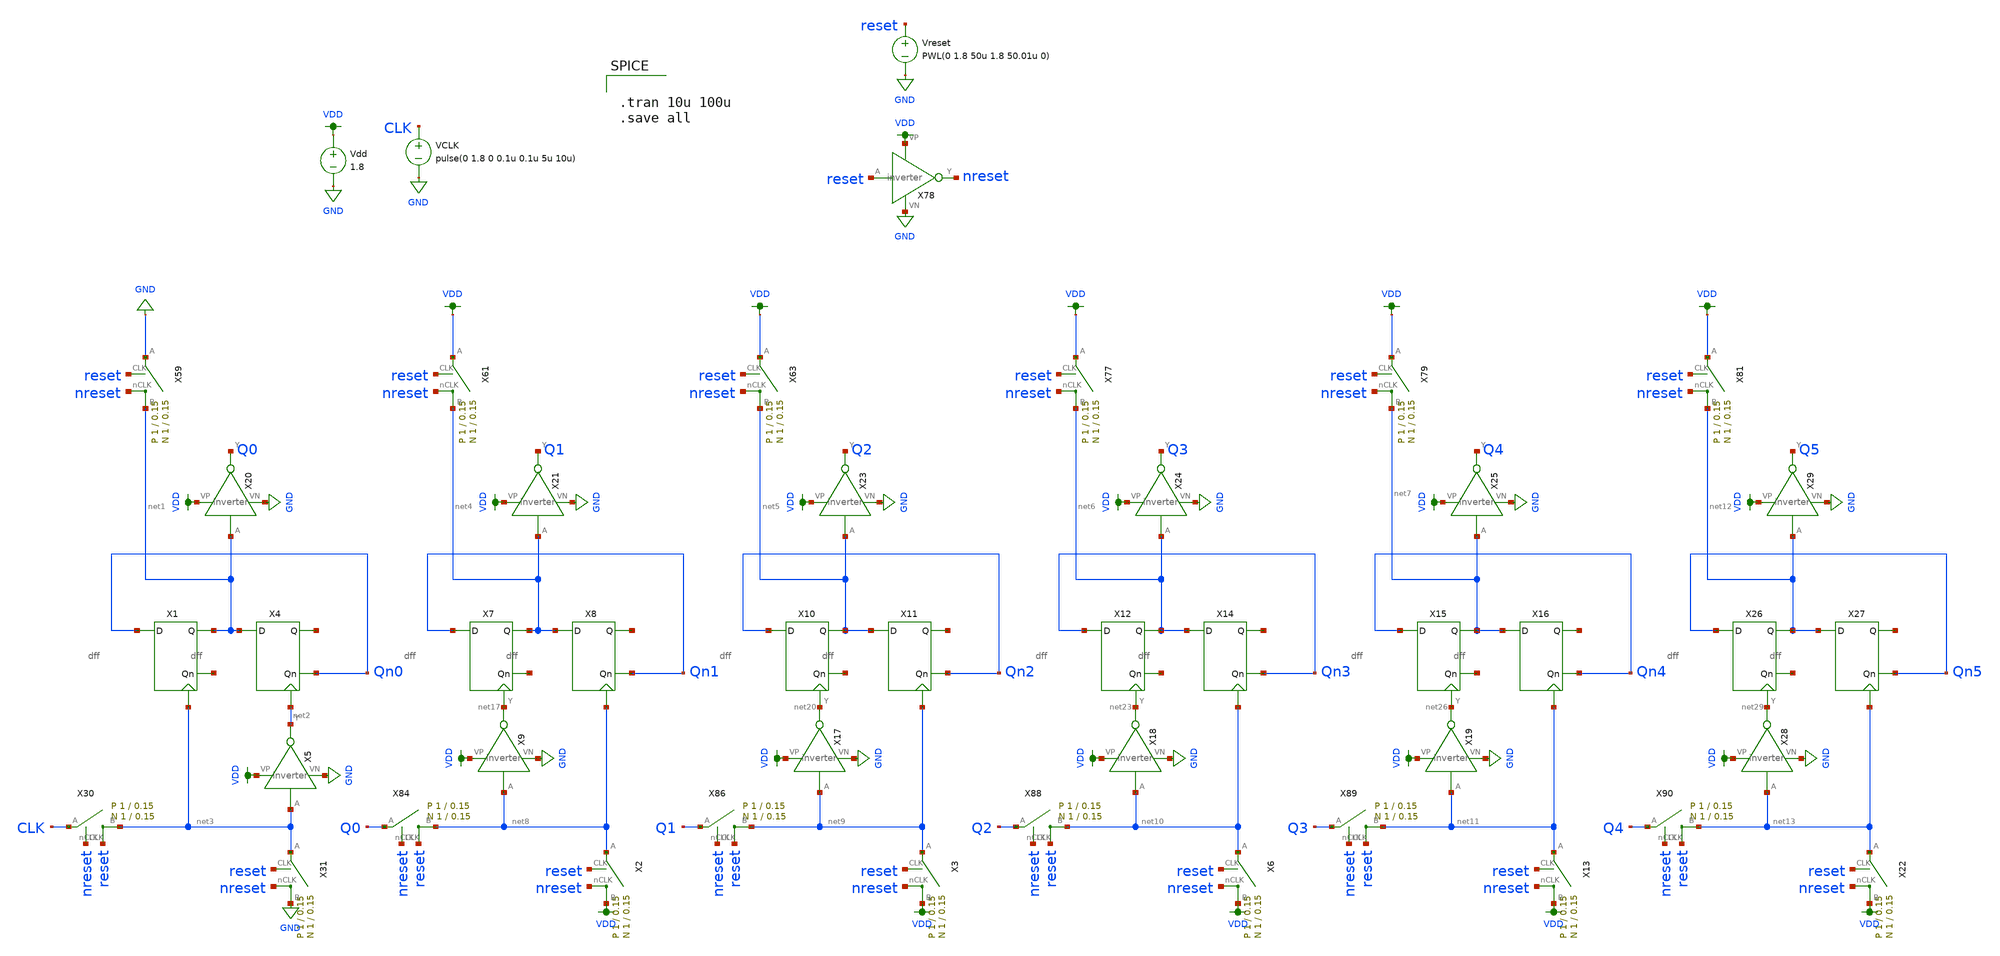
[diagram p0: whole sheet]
** sch_path: schematic/archive/counter_reset.sch
**.subckt counter_reset
Vdd VDD GND 1.8
VCLK CLK GND pulse(0 1.8 0 0.1u 0.1u 5u 10u)
X1 Qn0 net14 net1 net3 dff
X4 net1 Qn0 net15 net2 dff
X5 net3 net2 VDD GND inverter
X7 Qn1 net16 net4 net17 dff
X8 net4 Qn1 net18 net8 dff
X9 net8 net17 VDD GND inverter
X10 Qn2 net19 net5 net20 dff
X11 net5 Qn2 net21 net9 dff
X12 Qn3 net22 net6 net23 dff
X14 net6 Qn3 net24 net10 dff
X15 Qn4 net25 net7 net26 dff
X16 net7 Qn4 net27 net11 dff
X17 net9 net20 VDD GND inverter
X18 net10 net23 VDD GND inverter
X19 net11 net26 VDD GND inverter
X20 net1 Q0 VDD GND inverter
X21 net4 Q1 VDD GND inverter
X23 net5 Q2 VDD GND inverter
X24 net6 Q3 VDD GND inverter
X25 net7 Q4 VDD GND inverter
X26 Qn5 net28 net12 net29 dff
X27 net12 Qn5 net30 net13 dff
X28 net13 net29 VDD GND inverter
X29 net12 Q5 VDD GND inverter
X59 net1 GND reset nreset switch Wp=1 Lp=0.15 WW=1 LL=0.15
X61 net4 VDD reset nreset switch Wp=1 Lp=0.15 WW=1 LL=0.15
X63 net5 VDD reset nreset switch Wp=1 Lp=0.15 WW=1 LL=0.15
X77 net6 VDD reset nreset switch Wp=1 Lp=0.15 WW=1 LL=0.15
X79 net7 VDD reset nreset switch Wp=1 Lp=0.15 WW=1 LL=0.15
X81 net12 VDD reset nreset switch Wp=1 Lp=0.15 WW=1 LL=0.15
X84 net8 Q0 nreset reset switch Wp=1 Lp=0.15 WW=1 LL=0.15
X86 net9 Q1 nreset reset switch Wp=1 Lp=0.15 WW=1 LL=0.15
X88 net10 Q2 nreset reset switch Wp=1 Lp=0.15 WW=1 LL=0.15
X89 net11 Q3 nreset reset switch Wp=1 Lp=0.15 WW=1 LL=0.15
X90 net13 Q4 nreset reset switch Wp=1 Lp=0.15 WW=1 LL=0.15
Vreset reset GND PWL(0 1.8 50u 1.8 50.01u 0)
X78 reset nreset VDD GND inverter
X2 VDD net8 reset nreset switch Wp=1 Lp=0.15 WW=1 LL=0.15
X3 VDD net9 reset nreset switch Wp=1 Lp=0.15 WW=1 LL=0.15
X6 VDD net10 reset nreset switch Wp=1 Lp=0.15 WW=1 LL=0.15
X13 VDD net11 reset nreset switch Wp=1 Lp=0.15 WW=1 LL=0.15
X22 VDD net13 reset nreset switch Wp=1 Lp=0.15 WW=1 LL=0.15
X30 net3 CLK nreset reset switch Wp=1 Lp=0.15 WW=1 LL=0.15
X31 GND net3 reset nreset switch Wp=1 Lp=0.15 WW=1 LL=0.15
**** begin user architecture code


.tran 10u 100u
.save all


.option wnflag=1
.param MC_SWITCH=0.0
.lib ~/skywater/skywater-pdk/libraries/sky130_fd_pr_ngspice/latest/models/sky130.lib.spice tt

**** end user architecture code
**.ends

* expanding   symbol:  /home/madvlsi/Documents/MADVLSI-Final_Project/schematic/dff.sym # of pins=4
** sym_path: schematic/dff.sym
** sch_path: schematic/dff.sch
.subckt dff D Qn Q CLK
*.ipin D
*.iopin CLK
*.opin Qn
*.opin Q
X2 D CLK net1 VDD GND nand2
X3 net3 CLK net2 VDD GND nand2
X4 Q net2 Qn VDD GND nand2
X5 net1 Qn Q VDD GND nand2
X1 D net3 VDD GND inverter
.ends


* expanding   symbol:  /home/madvlsi/Documents/MADVLSI-Final_Project/schematic/inverter.sym # of
*+ pins=4
** sym_path: schematic/inverter.sym
** sch_path: schematic/inverter.sch
.subckt inverter A Y VP VN
*.opin Y
*.ipin A
*.iopin VP
*.iopin VN
XM3 Y A VP VDD sky130_fd_pr__pfet_01v8 L={Lp} W={Wp} nf=1 ad='int((nf+1)/2) * W/nf * 0.29' as='int((nf+2)/2) * W/nf * 0.29'
+ pd='2*int((nf+1)/2) * (W/nf + 0.29)' ps='2*int((nf+2)/2) * (W/nf + 0.29)' nrd='0.29 / W' nrs='0.29 / W'
+ sa=0 sb=0 sd=0 mult=1 m=1
XM4 Y A VP VDD sky130_fd_pr__pfet_01v8 L={Lp} W={Wp} nf=1 ad='int((nf+1)/2) * W/nf * 0.29' as='int((nf+2)/2) * W/nf * 0.29'
+ pd='2*int((nf+1)/2) * (W/nf + 0.29)' ps='2*int((nf+2)/2) * (W/nf + 0.29)' nrd='0.29 / W' nrs='0.29 / W'
+ sa=0 sb=0 sd=0 mult=1 m=1
XM5 Y A VN GND sky130_fd_pr__nfet_01v8 L={Lp} W={Wp} nf=1 ad='int((nf+1)/2) * W/nf * 0.29' as='int((nf+2)/2) * W/nf * 0.29'
+ pd='2*int((nf+1)/2) * (W/nf + 0.29)' ps='2*int((nf+2)/2) * (W/nf + 0.29)' nrd='0.29 / W' nrs='0.29 / W'
+ sa=0 sb=0 sd=0 mult=1 m=1
.ends


* expanding   symbol:  /home/madvlsi/Documents/MADVLSI-Final_Project/schematic/switch.sym # of
*+ pins=4
** sym_path: schematic/switch.sym
** sch_path: schematic/switch.sch
.subckt switch B A CLK nCLK  Wp=1 Lp=0.15 WW=1 LL=0.15
*.iopin B
*.iopin A
*.ipin CLK
*.ipin nCLK
*.ipin CLK
*.ipin CLK
*.ipin nCLK
*.ipin nCLK
XM1 A CLK B GND sky130_fd_pr__nfet_01v8 L={LL} W={WW} nf=1 ad='int((nf+1)/2) * W/nf * 0.29' as='int((nf+2)/2) * W/nf * 0.29'
+ pd='2*int((nf+1)/2) * (W/nf + 0.29)' ps='2*int((nf+2)/2) * (W/nf + 0.29)' nrd='0.29 / W' nrs='0.29 / W'
+ sa=0 sb=0 sd=0 mult=1 m=1
XM2 A nCLK B VDD sky130_fd_pr__pfet_01v8 L={Lp} W={Wp} nf=1 ad='int((nf+1)/2) * W/nf * 0.29' as='int((nf+2)/2) * W/nf * 0.29'
+ pd='2*int((nf+1)/2) * (W/nf + 0.29)' ps='2*int((nf+2)/2) * (W/nf + 0.29)' nrd='0.29 / W' nrs='0.29 / W'
+ sa=0 sb=0 sd=0 mult=1 m=1
XM3 B CLK B VDD sky130_fd_pr__pfet_01v8 L={Lp} W={Wp/2} nf=1 ad='int((nf+1)/2) * W/nf * 0.29' as='int((nf+2)/2) * W/nf * 0.29'
+ pd='2*int((nf+1)/2) * (W/nf + 0.29)' ps='2*int((nf+2)/2) * (W/nf + 0.29)' nrd='0.29 / W' nrs='0.29 / W'
+ sa=0 sb=0 sd=0 mult=1 m=1
XM4 A CLK A VDD sky130_fd_pr__pfet_01v8 L={Lp} W={Wp/2} nf=1 ad='int((nf+1)/2) * W/nf * 0.29' as='int((nf+2)/2) * W/nf * 0.29'
+ pd='2*int((nf+1)/2) * (W/nf + 0.29)' ps='2*int((nf+2)/2) * (W/nf + 0.29)' nrd='0.29 / W' nrs='0.29 / W'
+ sa=0 sb=0 sd=0 mult=1 m=1
XM5 B nCLK B GND sky130_fd_pr__nfet_01v8 L={LL} W={WW/2} nf=1 ad='int((nf+1)/2) * W/nf * 0.29' as='int((nf+2)/2) * W/nf * 0.29'
+ pd='2*int((nf+1)/2) * (W/nf + 0.29)' ps='2*int((nf+2)/2) * (W/nf + 0.29)' nrd='0.29 / W' nrs='0.29 / W'
+ sa=0 sb=0 sd=0 mult=1 m=1
XM6 A nCLK A GND sky130_fd_pr__nfet_01v8 L={LL} W={WW/2} nf=1 ad='int((nf+1)/2) * W/nf * 0.29' as='int((nf+2)/2) * W/nf * 0.29'
+ pd='2*int((nf+1)/2) * (W/nf + 0.29)' ps='2*int((nf+2)/2) * (W/nf + 0.29)' nrd='0.29 / W' nrs='0.29 / W'
+ sa=0 sb=0 sd=0 mult=1 m=1
.ends


* expanding   symbol:  /home/madvlsi/Documents/MADVLSI-Final_Project/schematic/nand2.sym # of pins=5
** sym_path: schematic/nand2.sym
** sch_path: schematic/nand2.sch
.subckt nand2 A B Y VP VN
*.ipin A
*.opin Y
*.ipin B
*.iopin VP
*.iopin VP
*.iopin VN
*.iopin VN
XM1 Y A VP VP sky130_fd_pr__pfet_01v8 L=0.15 W=2 nf=1 ad='int((nf+1)/2) * W/nf * 0.29' as='int((nf+2)/2) * W/nf * 0.29'
+ pd='2*int((nf+1)/2) * (W/nf + 0.29)' ps='2*int((nf+2)/2) * (W/nf + 0.29)' nrd='0.29 / W' nrs='0.29 / W'
+ sa=0 sb=0 sd=0 mult=1 m=1
XM2 VP B Y VP sky130_fd_pr__pfet_01v8 L=0.15 W=2 nf=1 ad='int((nf+1)/2) * W/nf * 0.29' as='int((nf+2)/2) * W/nf * 0.29'
+ pd='2*int((nf+1)/2) * (W/nf + 0.29)' ps='2*int((nf+2)/2) * (W/nf + 0.29)' nrd='0.29 / W' nrs='0.29 / W'
+ sa=0 sb=0 sd=0 mult=1 m=1
XM3 net1 B Y VN sky130_fd_pr__nfet_01v8 L=0.15 W=2 nf=1 ad='int((nf+1)/2) * W/nf * 0.29' as='int((nf+2)/2) * W/nf * 0.29'
+ pd='2*int((nf+1)/2) * (W/nf + 0.29)' ps='2*int((nf+2)/2) * (W/nf + 0.29)' nrd='0.29 / W' nrs='0.29 / W'
+ sa=0 sb=0 sd=0 mult=1 m=1
XM4 net1 A VN VN sky130_fd_pr__nfet_01v8 L=0.15 W=2 nf=1 ad='int((nf+1)/2) * W/nf * 0.29' as='int((nf+2)/2) * W/nf * 0.29'
+ pd='2*int((nf+1)/2) * (W/nf + 0.29)' ps='2*int((nf+2)/2) * (W/nf + 0.29)' nrd='0.29 / W' nrs='0.29 / W'
+ sa=0 sb=0 sd=0 mult=1 m=1
.ends

.GLOBAL GND
.GLOBAL VDD
.end
